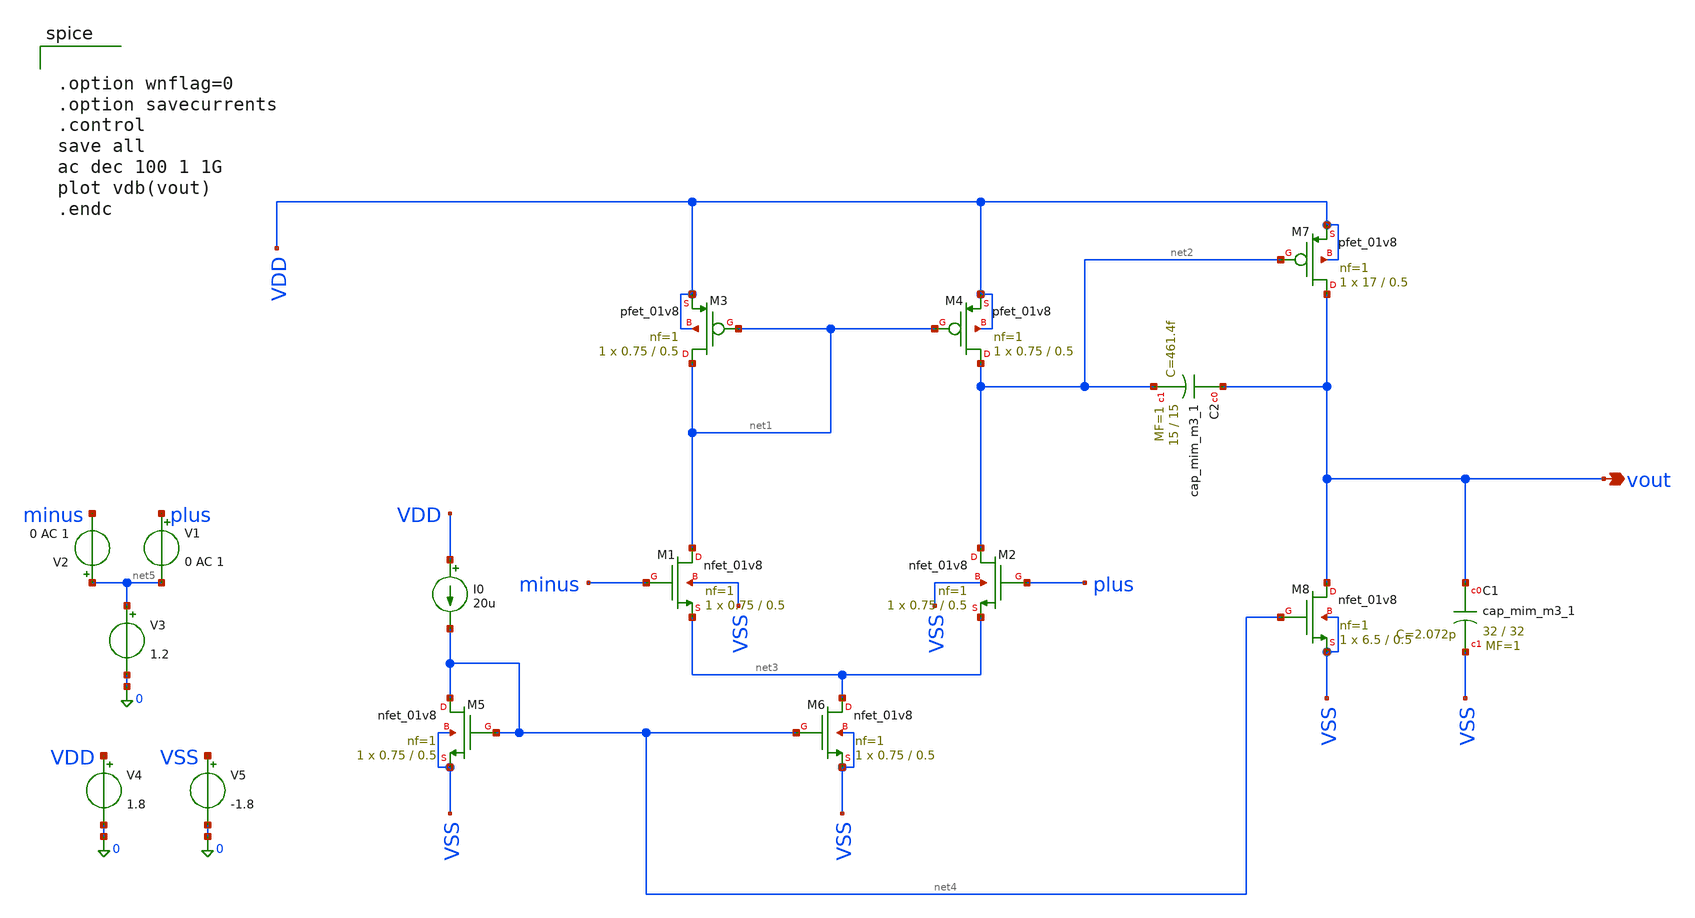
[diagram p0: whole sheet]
** sch_path: 2stageOTA_tb.sch
**.subckt 2stageOTA_tb vout
*.opin vout
I0 VDD net4 20u
V1 plus net5 0 AC 1
V2 net5 minus 0 AC 1
V3 net5 0 1.2
V4 VDD 0 1.8
V5 VSS 0 -1.8
XM1 net1 minus net3 VSS sky130_fd_pr__nfet_01v8 L=0.5 W=0.75 nf=1 ad='int((1 + 1)/2) * 0.75 / 1 * 0.29'
+ as='int((1 + 2)/2) * 0.75 / 1 * 0.29' pd='2*int((1 + 1)/2) * (0.75 / 1 + 0.29)' ps='2*int((1 + 2)/2) * (0.75 / 1 + 0.29)'
+ nrd='0.29 / 0.75 ' nrs='0.29 / 0.75 ' sa=0 sb=0 sd=0 mult=1 m=1
XM2 net2 plus net3 VSS sky130_fd_pr__nfet_01v8 L=0.5 W=0.75 nf=1 ad='int((1 + 1)/2) * 0.75 / 1 * 0.29'
+ as='int((1 + 2)/2) * 0.75 / 1 * 0.29' pd='2*int((1 + 1)/2) * (0.75 / 1 + 0.29)' ps='2*int((1 + 2)/2) * (0.75 / 1 + 0.29)'
+ nrd='0.29 / 0.75 ' nrs='0.29 / 0.75 ' sa=0 sb=0 sd=0 mult=1 m=1
XM3 net1 net1 VDD VDD sky130_fd_pr__pfet_01v8 L=0.5 W=0.75 nf=1 ad='int((1 + 1)/2) * 0.75 / 1 * 0.29'
+ as='int((1 + 2)/2) * 0.75 / 1 * 0.29' pd='2*int((1 + 1)/2) * (0.75 / 1 + 0.29)' ps='2*int((1 + 2)/2) * (0.75 / 1 + 0.29)'
+ nrd='0.29 / 0.75 ' nrs='0.29 / 0.75 ' sa=0 sb=0 sd=0 mult=1 m=1
XM4 net2 net1 VDD VDD sky130_fd_pr__pfet_01v8 L=0.5 W=0.75 nf=1 ad='int((1 + 1)/2) * 0.75 / 1 * 0.29'
+ as='int((1 + 2)/2) * 0.75 / 1 * 0.29' pd='2*int((1 + 1)/2) * (0.75 / 1 + 0.29)' ps='2*int((1 + 2)/2) * (0.75 / 1 + 0.29)'
+ nrd='0.29 / 0.75 ' nrs='0.29 / 0.75 ' sa=0 sb=0 sd=0 mult=1 m=1
XM5 net4 net4 VSS VSS sky130_fd_pr__nfet_01v8 L=0.5 W=0.75 nf=1 ad='int((1 + 1)/2) * 0.75 / 1 * 0.29'
+ as='int((1 + 2)/2) * 0.75 / 1 * 0.29' pd='2*int((1 + 1)/2) * (0.75 / 1 + 0.29)' ps='2*int((1 + 2)/2) * (0.75 / 1 + 0.29)'
+ nrd='0.29 / 0.75 ' nrs='0.29 / 0.75 ' sa=0 sb=0 sd=0 mult=1 m=1
XM6 net3 net4 VSS VSS sky130_fd_pr__nfet_01v8 L=0.5 W=0.75 nf=1 ad='int((1 + 1)/2) * 0.75 / 1 * 0.29'
+ as='int((1 + 2)/2) * 0.75 / 1 * 0.29' pd='2*int((1 + 1)/2) * (0.75 / 1 + 0.29)' ps='2*int((1 + 2)/2) * (0.75 / 1 + 0.29)'
+ nrd='0.29 / 0.75 ' nrs='0.29 / 0.75 ' sa=0 sb=0 sd=0 mult=1 m=1
XM7 vout net2 VDD VDD sky130_fd_pr__pfet_01v8 L=0.5 W=17 nf=1 ad='int((1 + 1)/2) * 17 / 1 * 0.29' as='int((1 + 2)/2) * 17 / 1 * 0.29'
+ pd='2*int((1 + 1)/2) * (17 / 1 + 0.29)' ps='2*int((1 + 2)/2) * (17 / 1 + 0.29)' nrd='0.29 / 17 ' nrs='0.29 / 17 '
+ sa=0 sb=0 sd=0 mult=1 m=1
XM8 vout net4 VSS VSS sky130_fd_pr__nfet_01v8 L=0.5 W=6.5 nf=1 ad='int((1 + 1)/2) * 6.5 / 1 * 0.29' as='int((1 + 2)/2) * 6.5 / 1 * 0.29'
+ pd='2*int((1 + 1)/2) * (6.5 / 1 + 0.29)' ps='2*int((1 + 2)/2) * (6.5 / 1 + 0.29)' nrd='0.29 / 6.5 ' nrs='0.29 / 6.5 '
+ sa=0 sb=0 sd=0 mult=1 m=1
XC2 vout net2 sky130_fd_pr__cap_mim_m3_1 W=15 L=15 MF=1 m=1
XC1 vout VSS sky130_fd_pr__cap_mim_m3_1 W=32 L=32 MF=1 m=1
**** begin user architecture code


.option wnflag=0
.option savecurrents
.control
save all
ac dec 100 1 1G
plot vdb(vout)
.endc



 .lib /foss/pdks/sky130A/libs.tech/ngspice/sky130.lib.spice tt

.param mc_mm_switch=0
.param mc_pr_switch=1

**** end user architecture code
**.ends
.end
